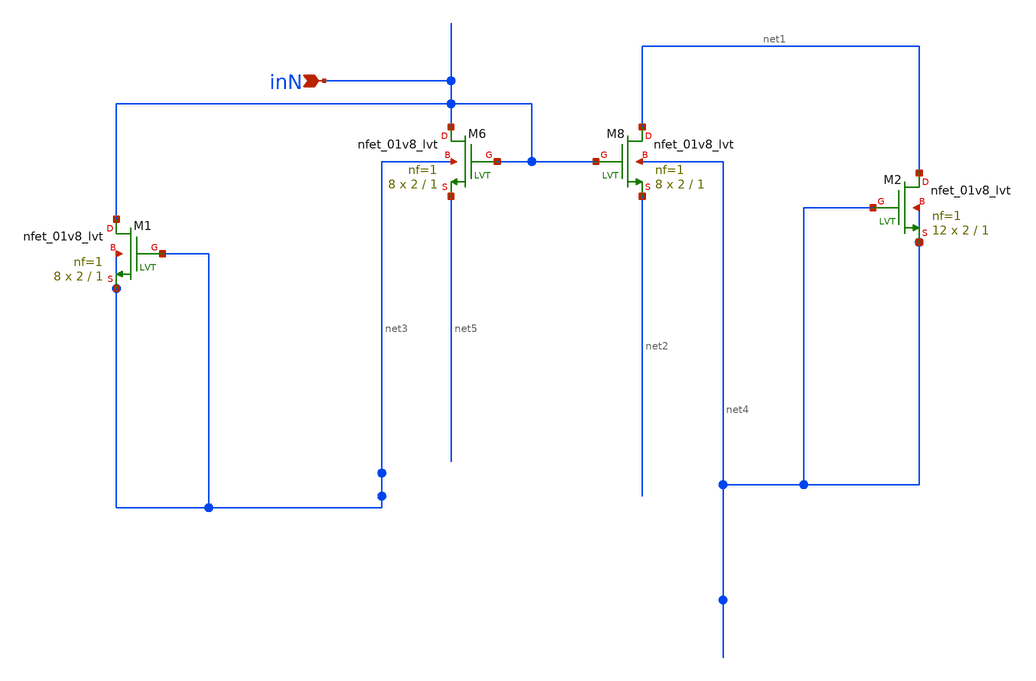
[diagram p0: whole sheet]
** sch_path: Current_mirror.sch
**.subckt Current_mirror inN
*.ipin inN
XM6 inN inN net5 net3 sky130_fd_pr__nfet_01v8_lvt L=1 W=2 nf=1 ad='int((1 + 1)/2) * 2 / 1 * 0.29' as='int((1 + 2)/2) * 2 / 1 * 0.29'
+ pd='2*int((1 + 1)/2) * (2 / 1 + 0.29)' ps='2*int((1 + 2)/2) * (2 / 1 + 0.29)' nrd='0.29 / 2 ' nrs='0.29 / 2 '
+ sa=0 sb=0 sd=0 mult=8 m=8
XM8 net1 inN net2 net4 sky130_fd_pr__nfet_01v8_lvt L=1 W=2 nf=1 ad='int((1 + 1)/2) * 2 / 1 * 0.29' as='int((1 + 2)/2) * 2 / 1 * 0.29'
+ pd='2*int((1 + 1)/2) * (2 / 1 + 0.29)' ps='2*int((1 + 2)/2) * (2 / 1 + 0.29)' nrd='0.29 / 2 ' nrs='0.29 / 2 '
+ sa=0 sb=0 sd=0 mult=8 m=8
XM1 inN net3 net3 net3 sky130_fd_pr__nfet_01v8_lvt L=1 W=2 nf=1 ad='int((1 + 1)/2) * 2 / 1 * 0.29' as='int((1 + 2)/2) * 2 / 1 * 0.29'
+ pd='2*int((1 + 1)/2) * (2 / 1 + 0.29)' ps='2*int((1 + 2)/2) * (2 / 1 + 0.29)' nrd='0.29 / 2 ' nrs='0.29 / 2 '
+ sa=0 sb=0 sd=0 mult=8 m=8
XM2 net1 net4 net4 net4 sky130_fd_pr__nfet_01v8_lvt L=1 W=2 nf=1 ad='int((1 + 1)/2) * 2 / 1 * 0.29' as='int((1 + 2)/2) * 2 / 1 * 0.29'
+ pd='2*int((1 + 1)/2) * (2 / 1 + 0.29)' ps='2*int((1 + 2)/2) * (2 / 1 + 0.29)' nrd='0.29 / 2 ' nrs='0.29 / 2 '
+ sa=0 sb=0 sd=0 mult=12 m=12
**.ends
.end
